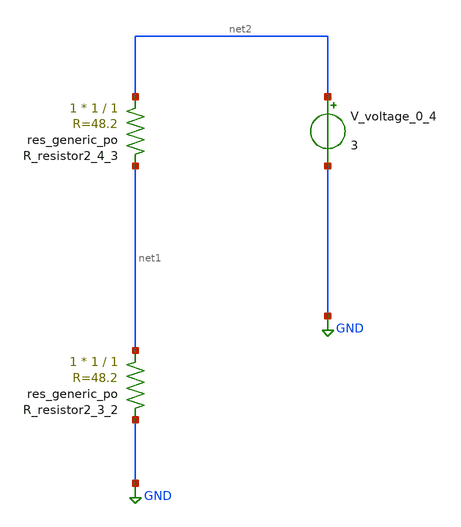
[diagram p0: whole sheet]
** sch_path: schematics/AMSNet/650.sch
**.subckt 650
XR_resistor2_3_2 net1 GND sky130_fd_pr__res_generic_po W=1 L=1 m=1
XR_resistor2_4_3 net2 net1 sky130_fd_pr__res_generic_po W=1 L=1 m=1
V_voltage_0_4 net2 GND 3
**.ends
.GLOBAL GND
.end
